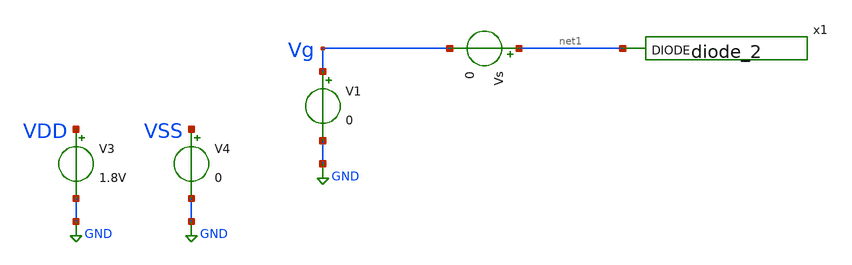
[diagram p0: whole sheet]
** sch_path: xschem/tests/dummy_tests/dummy_diode_std_cell.sch
**.subckt dummy_diode_std_cell
V3 VDD GND 1.8V
V4 VSS GND 0
V1 Vg GND 0
Vs net1 Vg 0
x1 net1 VGND VNB VPB VPWR sky130_fd_sc_hd__diode_2
**** begin user architecture code
 .lib $::SKYWATER_MODELS/sky130.lib.spice tt
.include $::SKYWATER_STDCELLS/sky130_fd_sc_hd.spice


.options acct list
.temp 25
*vvcc VDD 0 dc 1.8
*vvss VSS 0 0
.control
*tran 0.1u 400u
dc v1 0 10V 0.1
*plot RST_PLS clk+2 Pulse+4
plot Vg
plot i(Vs)
write pulse_generator_test.raw
.endc


**** end user architecture code
**.ends
.GLOBAL GND
.end
